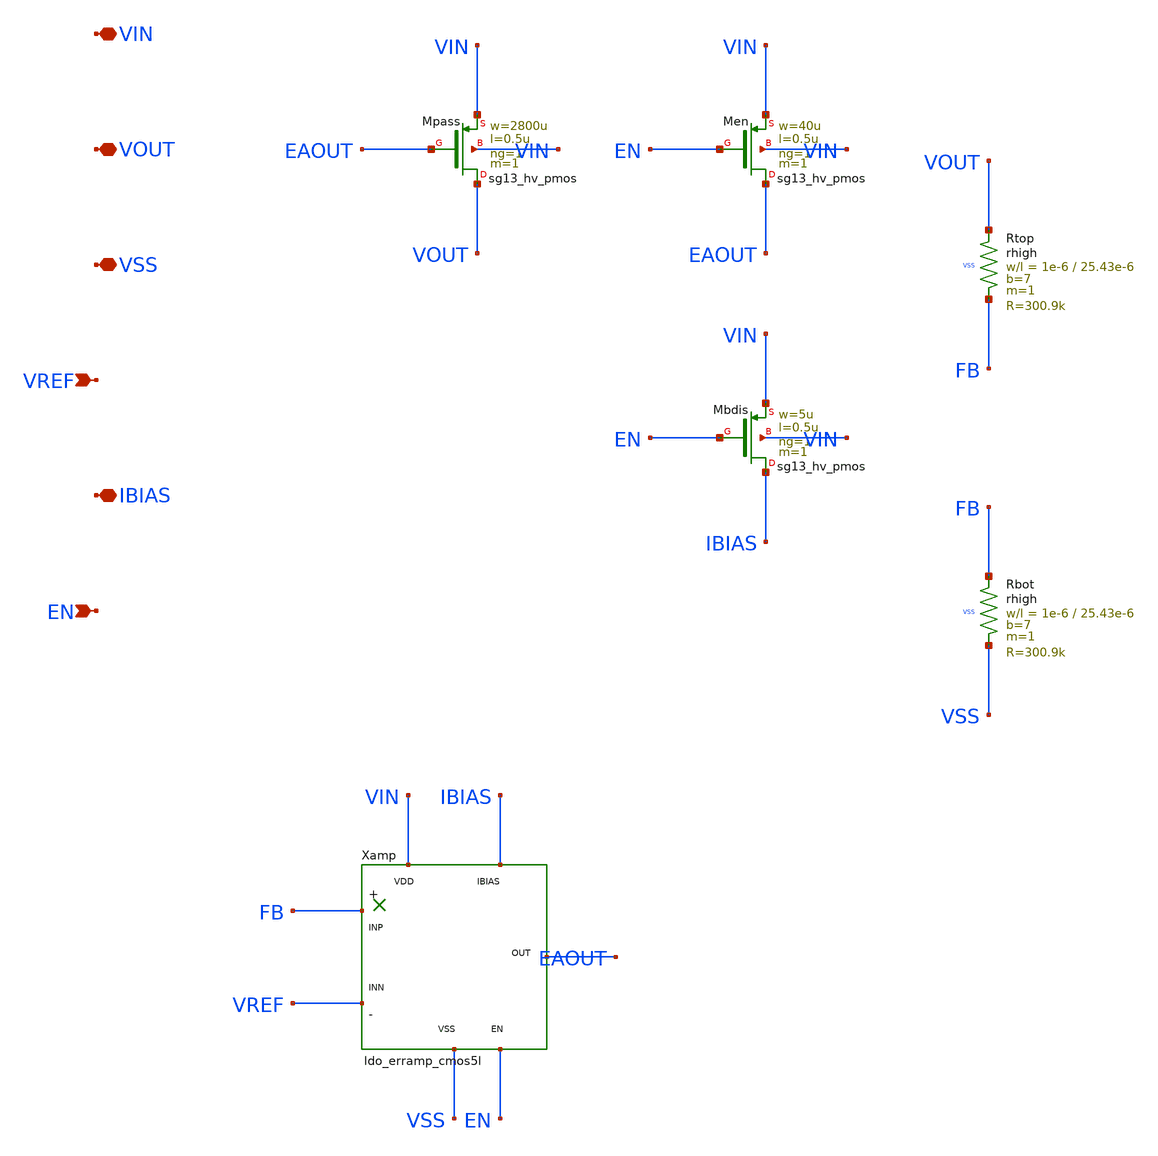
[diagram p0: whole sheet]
** sch_path: design/sg13cmos5l/ldo_core_cmos5l.sch
**.subckt ldo_core_cmos5l VIN VOUT VSS VREF IBIAS EN
*.iopin VIN
*.iopin VOUT
*.iopin VSS
*.ipin VREF
*.iopin IBIAS
*.ipin EN
XMpass VOUT EAOUT VIN VIN sg13_hv_pmos w=2800u l=0.5u ng=1 m=1 mm_ok=1
XRtop VOUT FB VSS rhigh w=1e-6 l=25.43e-6 m=1 b=7 mm_ok=1
XRbot FB VSS VSS rhigh w=1e-6 l=25.43e-6 m=1 b=7 mm_ok=1
Xamp FB VREF EAOUT VIN VSS IBIAS EN ldo_erramp_cmos5l
XMen EAOUT EN VIN VIN sg13_hv_pmos w=40u l=0.5u ng=1 m=1 mm_ok=1
XMbdis IBIAS EN VIN VIN sg13_hv_pmos w=5u l=0.5u ng=1 m=1 mm_ok=1
**.ends

* expanding   symbol:  ldo_erramp_cmos5l.sym # of pins=7
** sym_path: design/sg13cmos5l/ldo_erramp_cmos5l.sym
** sch_path: design/sg13cmos5l/ldo_erramp_cmos5l.sch
.subckt ldo_erramp_cmos5l INP INN OUT VDD VSS IBIAS EN
*.ipin INP
*.ipin INN
*.opin OUT
*.iopin VDD
*.iopin VSS
*.iopin IBIAS
*.ipin EN
XMb0 IBIAS IBIAS VDD VDD sg13_hv_pmos w=5u l=2u ng=1 m=1 mm_ok=1
XMtail TAIL IBIAS VDD VDD sg13_hv_pmos w=5u l=2u ng=1 m=3 mm_ok=1
XMload2 OUT IBIAS VDD VDD sg13_hv_pmos w=5u l=2u ng=1 m=6 mm_ok=1
XMinp G1 INP TAIL TAIL sg13_hv_pmos w=20u l=1u ng=1 m=1 mm_ok=1
XMinn N1 INN TAIL TAIL sg13_hv_pmos w=20u l=1u ng=1 m=1 mm_ok=1
XMn2 G1 N1 VSS VSS sg13_hv_nmos w=5u l=1u ng=1 m=1 mm_ok=1
XMn1 N1 N1 VSS VSS sg13_hv_nmos w=5u l=1u ng=1 m=1 mm_ok=1
XMn3 OUT G1 VSS VSS sg13_hv_nmos w=20u l=1u ng=1 m=1 mm_ok=1
XCc OUT MZ cap_cmomi w=170e-6 l=30e-6 mmin=1 mmax=4 feed=double subblock=0 m=1 mm_ok=1
XRz MZ G1 VSS rhigh w=1e-6 l=28.81e-6 m=1 b=39 mm_ok=1
XMinvp ENB EN VDD VDD sg13_hv_pmos w=1u l=1u ng=1 m=1 mm_ok=1
XMinvn ENB EN VSS VSS sg13_hv_nmos w=1u l=1u ng=1 m=1 mm_ok=1
XMpd G1 ENB VSS VSS sg13_hv_nmos w=1u l=1u ng=1 m=1 mm_ok=1
.ends

.end
